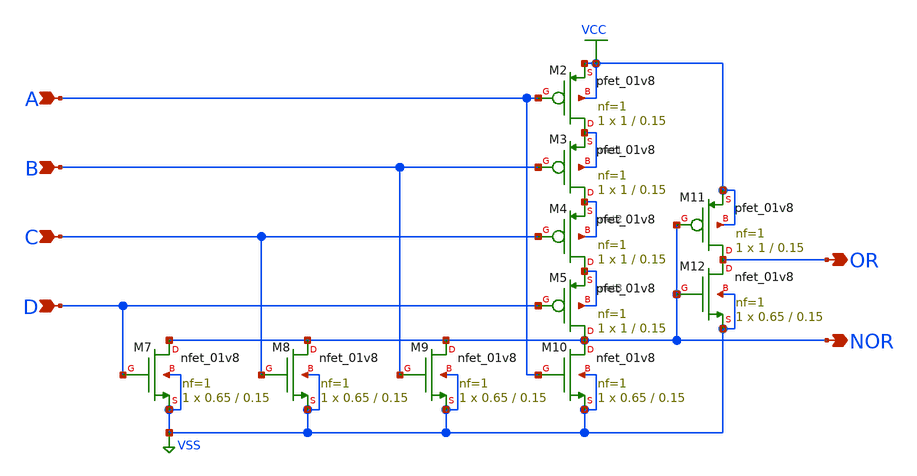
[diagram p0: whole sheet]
** sch_path: elements/logic/nor4.sch
**.subckt nor4 A NOR B C D OR
*.ipin A
*.opin NOR
*.ipin B
*.ipin C
*.ipin D
*.opin OR
XM2 net1 A VCC VCC sky130_fd_pr__pfet_01v8 L=0.15 W=1 nf=1 ad='int((nf+1)/2) * W/nf * 0.29' as='int((nf+2)/2) * W/nf * 0.29'
+ pd='2*int((nf+1)/2) * (W/nf + 0.29)' ps='2*int((nf+2)/2) * (W/nf + 0.29)' nrd='0.29 / W' nrs='0.29 / W'
+ sa=0 sb=0 sd=0 mult=1 m=1
XM3 net2 B net1 net1 sky130_fd_pr__pfet_01v8 L=0.15 W=1 nf=1 ad='int((nf+1)/2) * W/nf * 0.29' as='int((nf+2)/2) * W/nf * 0.29'
+ pd='2*int((nf+1)/2) * (W/nf + 0.29)' ps='2*int((nf+2)/2) * (W/nf + 0.29)' nrd='0.29 / W' nrs='0.29 / W'
+ sa=0 sb=0 sd=0 mult=1 m=1
XM4 net3 C net2 net2 sky130_fd_pr__pfet_01v8 L=0.15 W=1 nf=1 ad='int((nf+1)/2) * W/nf * 0.29' as='int((nf+2)/2) * W/nf * 0.29'
+ pd='2*int((nf+1)/2) * (W/nf + 0.29)' ps='2*int((nf+2)/2) * (W/nf + 0.29)' nrd='0.29 / W' nrs='0.29 / W'
+ sa=0 sb=0 sd=0 mult=1 m=1
XM5 NOR D net3 net3 sky130_fd_pr__pfet_01v8 L=0.15 W=1 nf=1 ad='int((nf+1)/2) * W/nf * 0.29' as='int((nf+2)/2) * W/nf * 0.29'
+ pd='2*int((nf+1)/2) * (W/nf + 0.29)' ps='2*int((nf+2)/2) * (W/nf + 0.29)' nrd='0.29 / W' nrs='0.29 / W'
+ sa=0 sb=0 sd=0 mult=1 m=1
XM7 NOR D VSS VSS sky130_fd_pr__nfet_01v8 L=0.15 W=0.65 nf=1 ad='int((1 + 1)/2) * 0.65 / 1 * 0.29' as='int((1 + 2)/2) * 0.65 / 1 * 0.29'
+ pd='2*int((1 + 1)/2) * (0.65 / 1 + 0.29)' ps='2*int((1 + 2)/2) * (0.65 / 1 + 0.29)' nrd='0.29 / 0.65 '
+ nrs='0.29 / 0.65 ' sa=0 sb=0 sd=0 mult=1 m=1
XM8 NOR C VSS VSS sky130_fd_pr__nfet_01v8 L=0.15 W=0.65 nf=1 ad='int((1 + 1)/2) * 0.65 / 1 * 0.29' as='int((1 + 2)/2) * 0.65 / 1 * 0.29'
+ pd='2*int((1 + 1)/2) * (0.65 / 1 + 0.29)' ps='2*int((1 + 2)/2) * (0.65 / 1 + 0.29)' nrd='0.29 / 0.65 '
+ nrs='0.29 / 0.65 ' sa=0 sb=0 sd=0 mult=1 m=1
XM9 NOR B VSS VSS sky130_fd_pr__nfet_01v8 L=0.15 W=0.65 nf=1 ad='int((1 + 1)/2) * 0.65 / 1 * 0.29' as='int((1 + 2)/2) * 0.65 / 1 * 0.29'
+ pd='2*int((1 + 1)/2) * (0.65 / 1 + 0.29)' ps='2*int((1 + 2)/2) * (0.65 / 1 + 0.29)' nrd='0.29 / 0.65 '
+ nrs='0.29 / 0.65 ' sa=0 sb=0 sd=0 mult=1 m=1
XM10 NOR A VSS VSS sky130_fd_pr__nfet_01v8 L=0.15 W=0.65 nf=1 ad='int((1 + 1)/2) * 0.65 / 1 * 0.29' as='int((1 + 2)/2) * 0.65 / 1 * 0.29'
+ pd='2*int((1 + 1)/2) * (0.65 / 1 + 0.29)' ps='2*int((1 + 2)/2) * (0.65 / 1 + 0.29)' nrd='0.29 / 0.65 '
+ nrs='0.29 / 0.65 ' sa=0 sb=0 sd=0 mult=1 m=1
XM11 OR NOR VCC VCC sky130_fd_pr__pfet_01v8 L=0.15 W=1 nf=1 ad='int((nf+1)/2) * W/nf * 0.29' as='int((nf+2)/2) * W/nf * 0.29'
+ pd='2*int((nf+1)/2) * (W/nf + 0.29)' ps='2*int((nf+2)/2) * (W/nf + 0.29)' nrd='0.29 / W' nrs='0.29 / W'
+ sa=0 sb=0 sd=0 mult=1 m=1
XM12 OR NOR VSS VSS sky130_fd_pr__nfet_01v8 L=0.15 W=0.65 nf=1 ad='int((1 + 1)/2) * 0.65 / 1 * 0.29'
+ as='int((1 + 2)/2) * 0.65 / 1 * 0.29' pd='2*int((1 + 1)/2) * (0.65 / 1 + 0.29)' ps='2*int((1 + 2)/2) * (0.65 / 1 + 0.29)'
+ nrd='0.29 / 0.65 ' nrs='0.29 / 0.65 ' sa=0 sb=0 sd=0 mult=1 m=1
**.ends
.GLOBAL VCC
.GLOBAL VSS
.end
